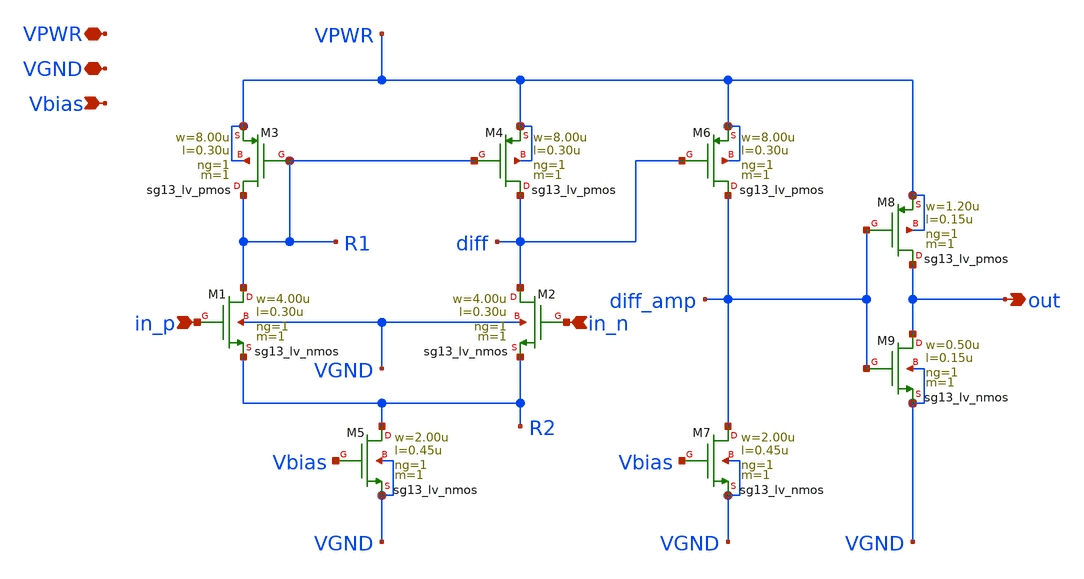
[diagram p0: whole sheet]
** sch_path: xschem/comparator.sch
**.subckt comparator VPWR in_p in_n out VGND Vbias
*.iopin VPWR
*.ipin in_p
*.ipin in_n
*.opin out
*.iopin VGND
*.ipin Vbias
XM1 R1 in_p R2 VGND sg13_lv_nmos w=4.00u l=0.30u ng=1 m=1 mm_ok=1
XM4 diff R1 VPWR VPWR sg13_lv_pmos w=8.00u l=0.30u ng=1 m=1 mm_ok=1
XM5 R2 Vbias VGND VGND sg13_lv_nmos w=2.00u l=0.45u ng=1 m=1 mm_ok=1
XM2 diff in_n R2 VGND sg13_lv_nmos w=4.00u l=0.30u ng=1 m=1 mm_ok=1
XM3 R1 R1 VPWR VPWR sg13_lv_pmos w=8.00u l=0.30u ng=1 m=1 mm_ok=1
XM6 diff_amp diff VPWR VPWR sg13_lv_pmos w=8.00u l=0.30u ng=1 m=1 mm_ok=1
XM7 diff_amp Vbias VGND VGND sg13_lv_nmos w=2.00u l=0.45u ng=1 m=1 mm_ok=1
XM8 out diff_amp VPWR VPWR sg13_lv_pmos w=1.20u l=0.15u ng=1 m=1 mm_ok=1
XM9 out diff_amp VGND VGND sg13_lv_nmos w=0.50u l=0.15u ng=1 m=1 mm_ok=1
**.ends
.end
